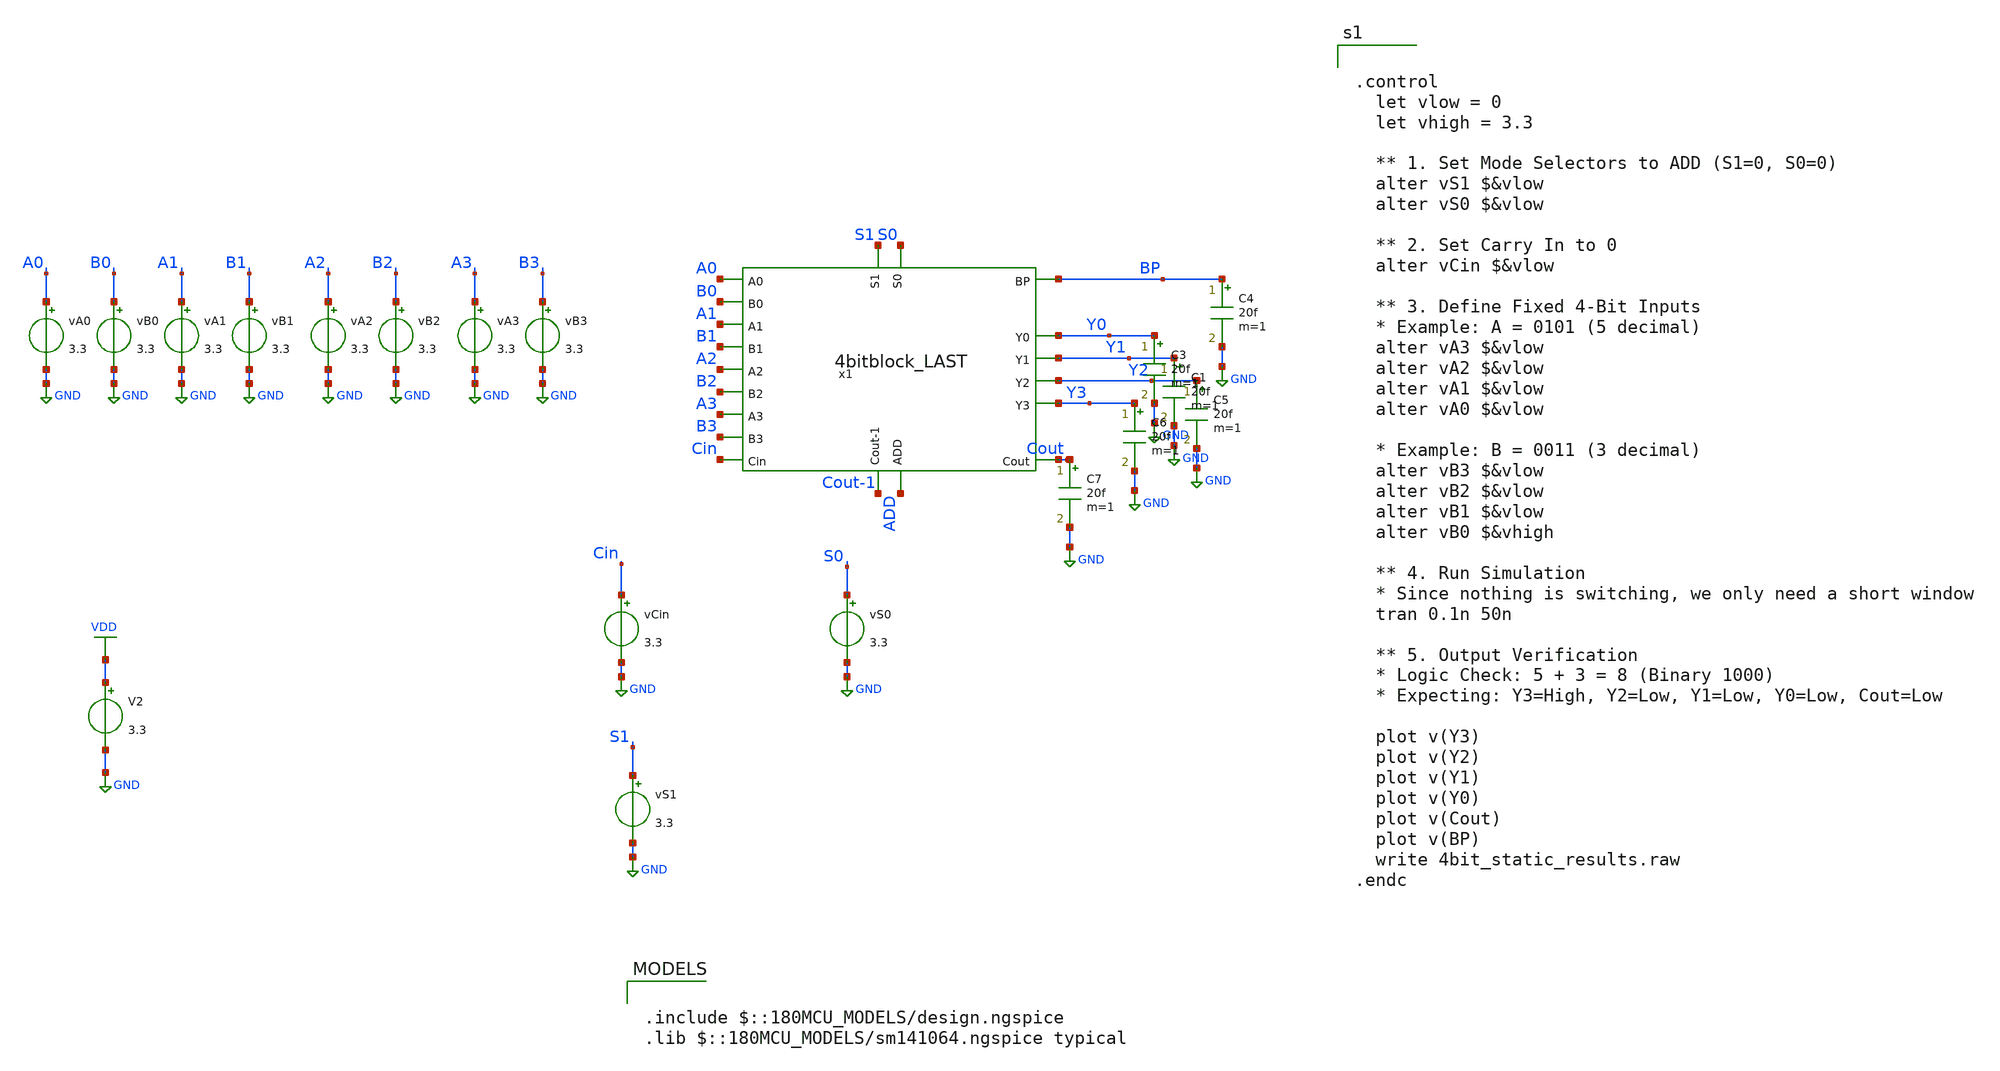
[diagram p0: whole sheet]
** sch_path: tbs/4bit_last.sch
**.subckt 4bit_last
vA0 A0 GND 3.3
vCin Cin GND 3.3
vS0 S0 GND 3.3
vB0 B0 GND 3.3
vS1 S1 GND 3.3
V2 VDD GND 3.3
vA1 A1 GND 3.3
vB1 B1 GND 3.3
vA2 A2 GND 3.3
vB2 B2 GND 3.3
vA3 A3 GND 3.3
vB3 B3 GND 3.3
C4 BP GND 20f m=1
C3 Y0 GND 20f m=1
C1 Y1 GND 20f m=1
C5 Y2 GND 20f m=1
C6 Y3 GND 20f m=1
C7 Cout GND 20f m=1
x1 ADD S0 BP S1 Cin Y1 Y0 Y3 Y2 A0 Cout B0 A1 B1 A2 B2 A3 B3 Cout-1 4bitblock_LAST
**** begin user architecture code

.include $::180MCU_MODELS/design.ngspice
.lib $::180MCU_MODELS/sm141064.ngspice typical



.control
  let vlow = 0
  let vhigh = 3.3

  ** 1. Set Mode Selectors to ADD (S1=0, S0=0)
  alter vS1 $&vlow
  alter vS0 $&vlow

  ** 2. Set Carry In to 0
  alter vCin $&vlow

  ** 3. Define Fixed 4-Bit Inputs
  * Example: A = 0101 (5 decimal)
  alter vA3 $&vlow
  alter vA2 $&vlow
  alter vA1 $&vlow
  alter vA0 $&vlow

  * Example: B = 0011 (3 decimal)
  alter vB3 $&vlow
  alter vB2 $&vlow
  alter vB1 $&vlow
  alter vB0 $&vhigh

  ** 4. Run Simulation
  * Since nothing is switching, we only need a short window
  tran 0.1n 50n

  ** 5. Output Verification
  * Logic Check: 5 + 3 = 8 (Binary 1000)
  * Expecting: Y3=High, Y2=Low, Y1=Low, Y0=Low, Cout=Low

  plot v(Y3)
  plot v(Y2)
  plot v(Y1)
  plot v(Y0)
  plot v(Cout)
  plot v(BP)
  write 4bit_static_results.raw
.endc


**** end user architecture code
**.ends
.GLOBAL GND
.GLOBAL VDD
.end
